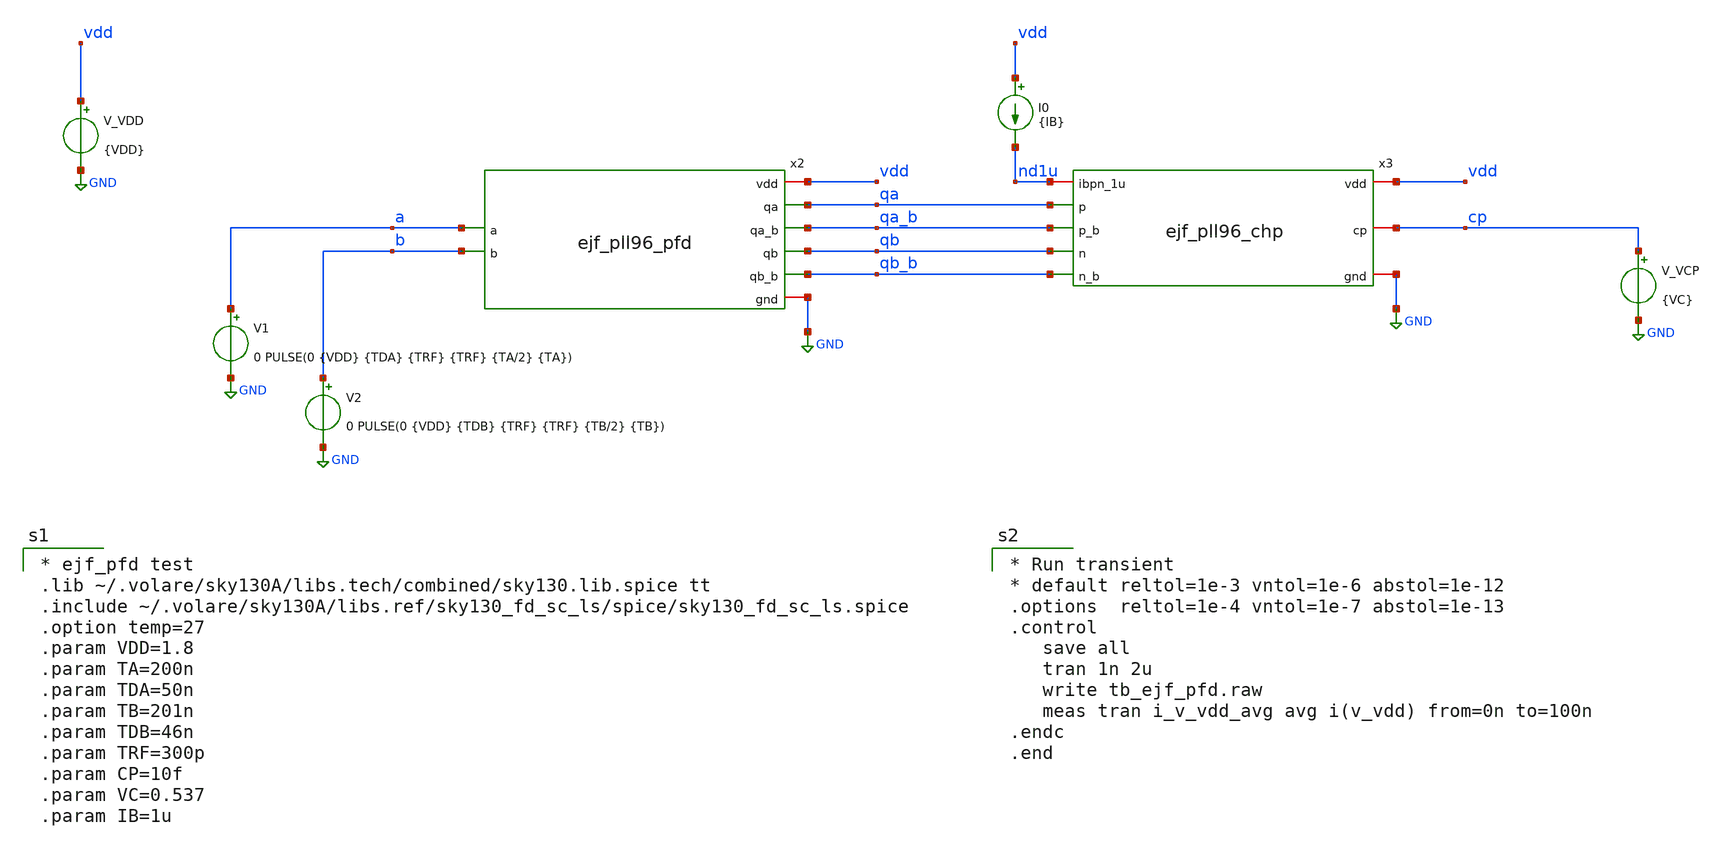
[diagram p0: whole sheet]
** sch_path: xschem/tb_ejf_pll96_pfd.sch
**.subckt tb_ejf_pll96_pfd
V_VDD vdd GND {VDD}
.save i(v_vdd)
V1 a GND 0 PULSE(0 {VDD} {TDA} {TRF} {TRF} {TA/2} {TA})
x2 qa a qb b vdd GND qa_b qb_b ejf_pll96_pfd
V2 b GND 0 PULSE(0 {VDD} {TDB} {TRF} {TRF} {TB/2} {TB})
x3 vdd qa_b qa cp nd1u qb_b qb GND ejf_pll96_chp
I0 vdd nd1u {IB}
V_VCP cp GND {VC}
.save i(v_vcp)
**** begin user architecture code

* ejf_pfd test
.lib ~/.volare/sky130A/libs.tech/combined/sky130.lib.spice tt
.include ~/.volare/sky130A/libs.ref/sky130_fd_sc_ls/spice/sky130_fd_sc_ls.spice
.option temp=27
.param VDD=1.8
.param TA=200n
.param TDA=50n
.param TB=201n
.param TDB=46n
.param TRF=300p
.param CP=10f
.param VC=0.537
.param IB=1u



* Run transient
* default reltol=1e-3 vntol=1e-6 abstol=1e-12
.options  reltol=1e-4 vntol=1e-7 abstol=1e-13
.control
   save all
   tran 1n 2u
   write tb_ejf_pfd.raw
   meas tran i_v_vdd_avg avg i(v_vdd) from=0n to=100n
.endc
.end

**** end user architecture code
**.ends

* expanding   symbol:  ejf_pll96_pfd.sym # of pins=8
** sym_path: xschem/ejf_pll96_pfd.sym
** sch_path: xschem/ejf_pll96_pfd.sch
.subckt ejf_pll96_pfd qa a qb b vdd gnd qa_b qb_b
*.iopin vdd
*.iopin gnd
*.ipin a
*.ipin b
*.opin qa
*.opin qb
*.opin qa_b
*.opin qb_b
x3 a_b b_b gnd gnd vdd vdd net1 sky130_fd_sc_ls__nor2_2
x4 net2 gnd gnd vdd vdd rst_b sky130_fd_sc_ls__clkinv_1
x1 a vdd rst_b gnd gnd vdd vdd qa0 sky130_fd_sc_ls__dfrtp_2
x2 b vdd rst_b gnd gnd vdd vdd qb0 sky130_fd_sc_ls__dfrtp_2
x6 vdd qa0 qa_b qa gnd a_b ejf_pll96_diff_buf
x7 vdd qb0 qb_b qb gnd b_b ejf_pll96_diff_buf
x8 b_b a_b gnd gnd vdd vdd net1 sky130_fd_sc_ls__nor2_2
x10 net1 gnd gnd vdd vdd net3 sky130_fd_sc_ls__dlygate4sd3_1
x5 net3 gnd gnd vdd vdd net2 sky130_fd_sc_ls__dlygate4sd3_1
.ends


* expanding   symbol:  ejf_pll96_chp.sym # of pins=8
** sym_path: xschem/ejf_pll96_chp.sym
** sch_path: xschem/ejf_pll96_chp.sch
.subckt ejf_pll96_chp vdd p_b p cp ibpn_1u n_b n gnd
*.iopin vdd
*.iopin gnd
*.iopin ibpn_1u
*.iopin cp
*.ipin p
*.ipin n_b
*.ipin p_b
*.ipin n
XMN3 net1 mn1g gnd gnd sky130_fd_pr__nfet_01v8 L=0.5 W=1 nf=1 ad='int((nf+1)/2) * W/nf * 0.29' as='int((nf+2)/2) * W/nf * 0.29'
+ pd='2*int((nf+1)/2) * (W/nf + 0.29)' ps='2*int((nf+2)/2) * (W/nf + 0.29)' nrd='0.29 / W' nrs='0.29 / W'
+ sa=0 sb=0 sd=0 mult=1 m=1
XMN3C mn1g ibpn_1u net1 gnd sky130_fd_pr__nfet_01v8 L=0.15 W=1 nf=1 ad='int((nf+1)/2) * W/nf * 0.29'
+ as='int((nf+2)/2) * W/nf * 0.29' pd='2*int((nf+1)/2) * (W/nf + 0.29)' ps='2*int((nf+2)/2) * (W/nf + 0.29)'
+ nrd='0.29 / W' nrs='0.29 / W' sa=0 sb=0 sd=0 mult=1 m=1
XMP2 net2 mp1g vdd vdd sky130_fd_pr__pfet_01v8 L=0.5 W=2 nf=1 ad='int((nf+1)/2) * W/nf * 0.29' as='int((nf+2)/2) * W/nf * 0.29'
+ pd='2*int((nf+1)/2) * (W/nf + 0.29)' ps='2*int((nf+2)/2) * (W/nf + 0.29)' nrd='0.29 / W' nrs='0.29 / W'
+ sa=0 sb=0 sd=0 mult=1 m=1
XMN2 net3 mn1g gnd gnd sky130_fd_pr__nfet_01v8 L=0.5 W=1 nf=1 ad='int((nf+1)/2) * W/nf * 0.29' as='int((nf+2)/2) * W/nf * 0.29'
+ pd='2*int((nf+1)/2) * (W/nf + 0.29)' ps='2*int((nf+2)/2) * (W/nf + 0.29)' nrd='0.29 / W' nrs='0.29 / W'
+ sa=0 sb=0 sd=0 mult=1 m=1
XMN2C mp1cg ibpn_1u net3 gnd sky130_fd_pr__nfet_01v8 L=0.15 W=1 nf=1 ad='int((nf+1)/2) * W/nf * 0.29'
+ as='int((nf+2)/2) * W/nf * 0.29' pd='2*int((nf+1)/2) * (W/nf + 0.29)' ps='2*int((nf+2)/2) * (W/nf + 0.29)'
+ nrd='0.29 / W' nrs='0.29 / W' sa=0 sb=0 sd=0 mult=1 m=1
XMP1 mp1d mp1g vdd vdd sky130_fd_pr__pfet_01v8 L=0.5 W=2 nf=1 ad='int((nf+1)/2) * W/nf * 0.29' as='int((nf+2)/2) * W/nf * 0.29'
+ pd='2*int((nf+1)/2) * (W/nf + 0.29)' ps='2*int((nf+2)/2) * (W/nf + 0.29)' nrd='0.29 / W' nrs='0.29 / W'
+ sa=0 sb=0 sd=0 mult=5 m=5
XMP2C mp1g mp1cg net2 vdd sky130_fd_pr__pfet_01v8 L=0.15 W=2 nf=1 ad='int((nf+1)/2) * W/nf * 0.29' as='int((nf+2)/2) * W/nf * 0.29'
+ pd='2*int((nf+1)/2) * (W/nf + 0.29)' ps='2*int((nf+2)/2) * (W/nf + 0.29)' nrd='0.29 / W' nrs='0.29 / W'
+ sa=0 sb=0 sd=0 mult=1 m=1
XMP1C mp1cd mp1cg mp1d vdd sky130_fd_pr__pfet_01v8 L=0.15 W=2 nf=1 ad='int((nf+1)/2) * W/nf * 0.29' as='int((nf+2)/2) * W/nf * 0.29'
+ pd='2*int((nf+1)/2) * (W/nf + 0.29)' ps='2*int((nf+2)/2) * (W/nf + 0.29)' nrd='0.29 / W' nrs='0.29 / W'
+ sa=0 sb=0 sd=0 mult=5 m=5
XMN1 mn1d mn1g gnd gnd sky130_fd_pr__nfet_01v8 L=0.5 W=1 nf=1 ad='int((nf+1)/2) * W/nf * 0.29' as='int((nf+2)/2) * W/nf * 0.29'
+ pd='2*int((nf+1)/2) * (W/nf + 0.29)' ps='2*int((nf+2)/2) * (W/nf + 0.29)' nrd='0.29 / W' nrs='0.29 / W'
+ sa=0 sb=0 sd=0 mult=5 m=5
XM1C mn1cd ibpn_1u mn1d gnd sky130_fd_pr__nfet_01v8 L=0.15 W=1 nf=1 ad='int((nf+1)/2) * W/nf * 0.29'
+ as='int((nf+2)/2) * W/nf * 0.29' pd='2*int((nf+1)/2) * (W/nf + 0.29)' ps='2*int((nf+2)/2) * (W/nf + 0.29)'
+ nrd='0.29 / W' nrs='0.29 / W' sa=0 sb=0 sd=0 mult=5 m=5
XR1 mn1g net4 gnd sky130_fd_pr__res_xhigh_po W=0.35 L=10 mult=1 m=1
XR2 net4 ibpn_1u gnd sky130_fd_pr__res_xhigh_po W=0.35 L=10 mult=1 m=1
XR3 mp1cg net5 vdd sky130_fd_pr__res_xhigh_po W=0.35 L=10 mult=1 m=1
XR4 net5 mp1g vdd sky130_fd_pr__res_xhigh_po W=0.35 L=10 mult=1 m=1
XMP11 cp_replica p mp1cd vdd sky130_fd_pr__pfet_01v8 L=0.15 W=1 nf=1 ad='int((nf+1)/2) * W/nf * 0.29'
+ as='int((nf+2)/2) * W/nf * 0.29' pd='2*int((nf+1)/2) * (W/nf + 0.29)' ps='2*int((nf+2)/2) * (W/nf + 0.29)'
+ nrd='0.29 / W' nrs='0.29 / W' sa=0 sb=0 sd=0 mult=1 m=1
XMN11 cp_replica n_b mn1cd gnd sky130_fd_pr__nfet_01v8 L=0.15 W=1 nf=1 ad='int((nf+1)/2) * W/nf * 0.29'
+ as='int((nf+2)/2) * W/nf * 0.29' pd='2*int((nf+1)/2) * (W/nf + 0.29)' ps='2*int((nf+2)/2) * (W/nf + 0.29)'
+ nrd='0.29 / W' nrs='0.29 / W' sa=0 sb=0 sd=0 mult=1 m=1
XMP10 cp p_b mp1cd vdd sky130_fd_pr__pfet_01v8 L=0.15 W=1 nf=1 ad='int((nf+1)/2) * W/nf * 0.29' as='int((nf+2)/2) * W/nf * 0.29'
+ pd='2*int((nf+1)/2) * (W/nf + 0.29)' ps='2*int((nf+2)/2) * (W/nf + 0.29)' nrd='0.29 / W' nrs='0.29 / W'
+ sa=0 sb=0 sd=0 mult=1 m=1
XMN10 cp n mn1cd gnd sky130_fd_pr__nfet_01v8 L=0.15 W=1 nf=1 ad='int((nf+1)/2) * W/nf * 0.29' as='int((nf+2)/2) * W/nf * 0.29'
+ pd='2*int((nf+1)/2) * (W/nf + 0.29)' ps='2*int((nf+2)/2) * (W/nf + 0.29)' nrd='0.29 / W' nrs='0.29 / W'
+ sa=0 sb=0 sd=0 mult=1 m=1
XMN4CAP gnd mn1g gnd gnd sky130_fd_pr__nfet_01v8 L=0.5 W=1 nf=1 ad='int((nf+1)/2) * W/nf * 0.29' as='int((nf+2)/2) * W/nf * 0.29'
+ pd='2*int((nf+1)/2) * (W/nf + 0.29)' ps='2*int((nf+2)/2) * (W/nf + 0.29)' nrd='0.29 / W' nrs='0.29 / W'
+ sa=0 sb=0 sd=0 mult=7 m=7
XMP4CAP vdd mp1g vdd vdd sky130_fd_pr__pfet_01v8 L=0.5 W=2 nf=1 ad='int((nf+1)/2) * W/nf * 0.29' as='int((nf+2)/2) * W/nf * 0.29'
+ pd='2*int((nf+1)/2) * (W/nf + 0.29)' ps='2*int((nf+2)/2) * (W/nf + 0.29)' nrd='0.29 / W' nrs='0.29 / W'
+ sa=0 sb=0 sd=0 mult=6 m=6
XMP5CAP vdd mp1cg vdd vdd sky130_fd_pr__pfet_01v8 L=0.5 W=2 nf=1 ad='int((nf+1)/2) * W/nf * 0.29' as='int((nf+2)/2) * W/nf * 0.29'
+ pd='2*int((nf+1)/2) * (W/nf + 0.29)' ps='2*int((nf+2)/2) * (W/nf + 0.29)' nrd='0.29 / W' nrs='0.29 / W'
+ sa=0 sb=0 sd=0 mult=6 m=6
XMN5CAP gnd ibpn_1u gnd gnd sky130_fd_pr__nfet_01v8 L=0.5 W=1 nf=1 ad='int((nf+1)/2) * W/nf * 0.29' as='int((nf+2)/2) * W/nf * 0.29'
+ pd='2*int((nf+1)/2) * (W/nf + 0.29)' ps='2*int((nf+2)/2) * (W/nf + 0.29)' nrd='0.29 / W' nrs='0.29 / W'
+ sa=0 sb=0 sd=0 mult=7 m=7
XMP3 mp3d mp1g vdd vdd sky130_fd_pr__pfet_01v8 L=0.5 W=2 nf=1 ad='int((nf+1)/2) * W/nf * 0.29' as='int((nf+2)/2) * W/nf * 0.29'
+ pd='2*int((nf+1)/2) * (W/nf + 0.29)' ps='2*int((nf+2)/2) * (W/nf + 0.29)' nrd='0.29 / W' nrs='0.29 / W'
+ sa=0 sb=0 sd=0 mult=2 m=2
XMN6 cp_replica ibpn_1u net6 gnd sky130_fd_pr__nfet_01v8 L=0.15 W=1 nf=1 ad='int((nf+1)/2) * W/nf * 0.29'
+ as='int((nf+2)/2) * W/nf * 0.29' pd='2*int((nf+1)/2) * (W/nf + 0.29)' ps='2*int((nf+2)/2) * (W/nf + 0.29)'
+ nrd='0.29 / W' nrs='0.29 / W' sa=0 sb=0 sd=0 mult=1 m=1
XMN7 ng ibpn_1u net7 gnd sky130_fd_pr__nfet_01v8 L=0.15 W=1 nf=1 ad='int((nf+1)/2) * W/nf * 0.29' as='int((nf+2)/2) * W/nf * 0.29'
+ pd='2*int((nf+1)/2) * (W/nf + 0.29)' ps='2*int((nf+2)/2) * (W/nf + 0.29)' nrd='0.29 / W' nrs='0.29 / W'
+ sa=0 sb=0 sd=0 mult=1 m=1
XC2 cp_replica gnd sky130_fd_pr__cap_mim_m3_1 W=14 L=14 MF=1 m=1
XM1 cp_replica cp_replica mp3d VDD sky130_fd_pr__pfet_01v8_lvt L=0.35 W=4 nf=2 ad='int((nf+1)/2) * W/nf * 0.29'
+ as='int((nf+2)/2) * W/nf * 0.29' pd='2*int((nf+1)/2) * (W/nf + 0.29)' ps='2*int((nf+2)/2) * (W/nf + 0.29)'
+ nrd='0.29 / W' nrs='0.29 / W' sa=0 sb=0 sd=0 mult=1 m=1
XM2 ng cp mp3d VDD sky130_fd_pr__pfet_01v8_lvt L=0.35 W=4 nf=2 ad='int((nf+1)/2) * W/nf * 0.29' as='int((nf+2)/2) * W/nf * 0.29'
+ pd='2*int((nf+1)/2) * (W/nf + 0.29)' ps='2*int((nf+2)/2) * (W/nf + 0.29)' nrd='0.29 / W' nrs='0.29 / W'
+ sa=0 sb=0 sd=0 mult=1 m=1
XM3 net7 ng gnd GND sky130_fd_pr__nfet_01v8_lvt L=0.35 W=2 nf=2 ad='int((nf+1)/2) * W/nf * 0.29' as='int((nf+2)/2) * W/nf * 0.29'
+ pd='2*int((nf+1)/2) * (W/nf + 0.29)' ps='2*int((nf+2)/2) * (W/nf + 0.29)' nrd='0.29 / W' nrs='0.29 / W'
+ sa=0 sb=0 sd=0 mult=1 m=1
XM4 net6 ng gnd GND sky130_fd_pr__nfet_01v8_lvt L=0.35 W=2 nf=2 ad='int((nf+1)/2) * W/nf * 0.29' as='int((nf+2)/2) * W/nf * 0.29'
+ pd='2*int((nf+1)/2) * (W/nf + 0.29)' ps='2*int((nf+2)/2) * (W/nf + 0.29)' nrd='0.29 / W' nrs='0.29 / W'
+ sa=0 sb=0 sd=0 mult=1 m=1
C1 vdd mp1g 1u m=1
C3 vdd mp1cg 1u m=1
C4 ibpn_1u gnd 1u m=1
C5 ibpn_1u gnd 1u m=1
C6 cp_replica gnd 1u m=1
.ends


* expanding   symbol:  ejf_pll96_diff_buf.sym # of pins=6
** sym_path: xschem/ejf_pll96_diff_buf.sym
** sch_path: xschem/ejf_pll96_diff_buf.sch
.subckt ejf_pll96_diff_buf vdd a y_b y gnd a_b
*.iopin vdd
*.iopin gnd
*.ipin a
*.opin y_b
*.opin y
*.opin a_b
XM11 a_b a gnd gnd sky130_fd_pr__nfet_01v8 L=0.15 W=0.84 nf=2 ad='int((nf+1)/2) * W/nf * 0.29' as='int((nf+2)/2) * W/nf * 0.29'
+ pd='2*int((nf+1)/2) * (W/nf + 0.29)' ps='2*int((nf+2)/2) * (W/nf + 0.29)' nrd='0.29 / W' nrs='0.29 / W'
+ sa=0 sb=0 sd=0 mult=1 m=1
XM12 a_b a vdd vdd sky130_fd_pr__pfet_01v8_hvt L=0.15 W=3.36 nf=3 ad='int((nf+1)/2) * W/nf * 0.29' as='int((nf+2)/2) * W/nf * 0.29'
+ pd='2*int((nf+1)/2) * (W/nf + 0.29)' ps='2*int((nf+2)/2) * (W/nf + 0.29)' nrd='0.29 / W' nrs='0.29 / W'
+ sa=0 sb=0 sd=0 mult=1 m=1
XM1 y_b net1 gnd gnd sky130_fd_pr__nfet_01v8 L=0.15 W=0.84 nf=2 ad='int((nf+1)/2) * W/nf * 0.29' as='int((nf+2)/2) * W/nf * 0.29'
+ pd='2*int((nf+1)/2) * (W/nf + 0.29)' ps='2*int((nf+2)/2) * (W/nf + 0.29)' nrd='0.29 / W' nrs='0.29 / W'
+ sa=0 sb=0 sd=0 mult=1 m=1
XM2 y_b net1 vdd vdd sky130_fd_pr__pfet_01v8_hvt L=0.15 W=3.36 nf=3 ad='int((nf+1)/2) * W/nf * 0.29'
+ as='int((nf+2)/2) * W/nf * 0.29' pd='2*int((nf+1)/2) * (W/nf + 0.29)' ps='2*int((nf+2)/2) * (W/nf + 0.29)'
+ nrd='0.29 / W' nrs='0.29 / W' sa=0 sb=0 sd=0 mult=1 m=1
XM3 net1 a_b gnd gnd sky130_fd_pr__nfet_01v8 L=0.15 W=0.84 nf=2 ad='int((nf+1)/2) * W/nf * 0.29' as='int((nf+2)/2) * W/nf * 0.29'
+ pd='2*int((nf+1)/2) * (W/nf + 0.29)' ps='2*int((nf+2)/2) * (W/nf + 0.29)' nrd='0.29 / W' nrs='0.29 / W'
+ sa=0 sb=0 sd=0 mult=1 m=1
XM4 net1 a_b vdd vdd sky130_fd_pr__pfet_01v8_hvt L=0.15 W=3.36 nf=3 ad='int((nf+1)/2) * W/nf * 0.29'
+ as='int((nf+2)/2) * W/nf * 0.29' pd='2*int((nf+1)/2) * (W/nf + 0.29)' ps='2*int((nf+2)/2) * (W/nf + 0.29)'
+ nrd='0.29 / W' nrs='0.29 / W' sa=0 sb=0 sd=0 mult=1 m=1
XM5 y net2 gnd gnd sky130_fd_pr__nfet_01v8 L=0.15 W=0.84 nf=2 ad='int((nf+1)/2) * W/nf * 0.29' as='int((nf+2)/2) * W/nf * 0.29'
+ pd='2*int((nf+1)/2) * (W/nf + 0.29)' ps='2*int((nf+2)/2) * (W/nf + 0.29)' nrd='0.29 / W' nrs='0.29 / W'
+ sa=0 sb=0 sd=0 mult=1 m=1
XM6 y net2 vdd vdd sky130_fd_pr__pfet_01v8_hvt L=0.15 W=3.36 nf=3 ad='int((nf+1)/2) * W/nf * 0.29' as='int((nf+2)/2) * W/nf * 0.29'
+ pd='2*int((nf+1)/2) * (W/nf + 0.29)' ps='2*int((nf+2)/2) * (W/nf + 0.29)' nrd='0.29 / W' nrs='0.29 / W'
+ sa=0 sb=0 sd=0 mult=1 m=1
XM9 net2 gnd a_b VDD sky130_fd_pr__pfet_01v8_hvt L=0.15 W=3.36 nf=3 ad='int((nf+1)/2) * W/nf * 0.29'
+ as='int((nf+2)/2) * W/nf * 0.29' pd='2*int((nf+1)/2) * (W/nf + 0.29)' ps='2*int((nf+2)/2) * (W/nf + 0.29)'
+ nrd='0.29 / W' nrs='0.29 / W' sa=0 sb=0 sd=0 mult=1 m=1
XM10 net2 vdd a_b GND sky130_fd_pr__nfet_01v8 L=0.15 W=0.84 nf=2 ad='int((nf+1)/2) * W/nf * 0.29' as='int((nf+2)/2) * W/nf * 0.29'
+ pd='2*int((nf+1)/2) * (W/nf + 0.29)' ps='2*int((nf+2)/2) * (W/nf + 0.29)' nrd='0.29 / W' nrs='0.29 / W'
+ sa=0 sb=0 sd=0 mult=1 m=1
.ends

.GLOBAL GND
.end
